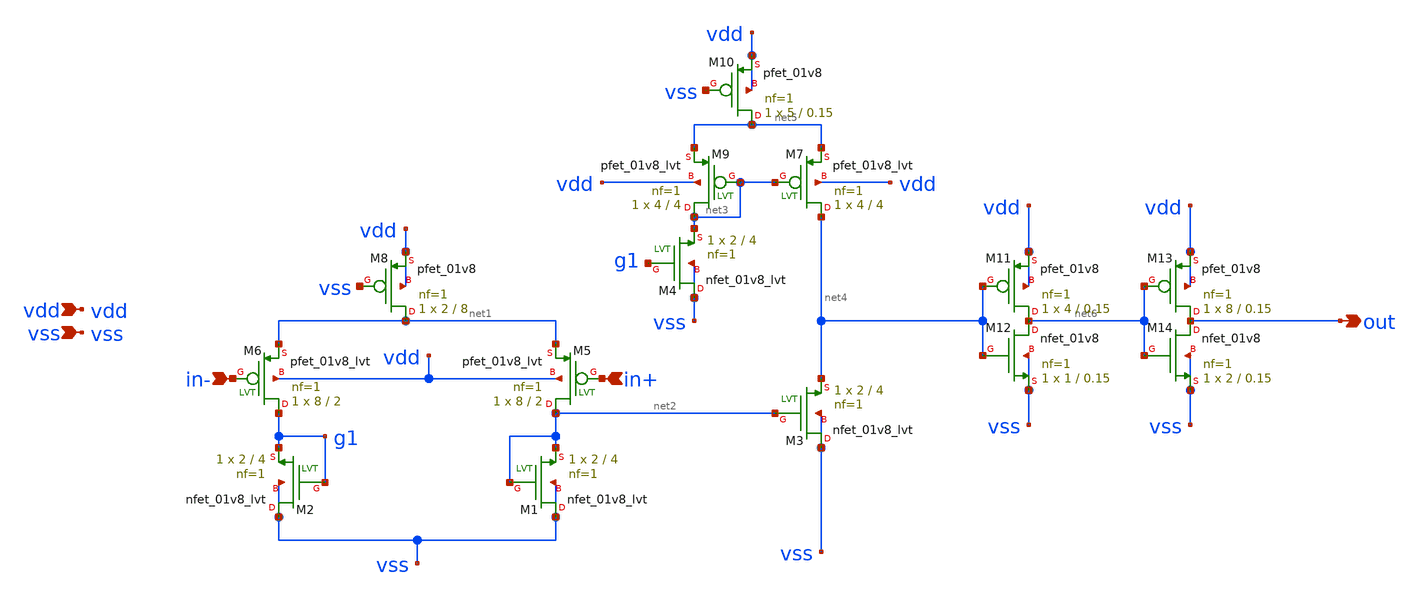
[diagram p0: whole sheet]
** sch_path: custom_gds/tt_um_tim2305_adc_dac/xschem/compr2.sch
**.subckt compr2 in- out in+ vdd vss
*.ipin in-
*.opin out
*.ipin in+
*.ipin vdd
*.ipin vss
XM1 vss net2 net2 vss sky130_fd_pr__nfet_01v8_lvt L=4 W=2 nf=1 ad='int((nf+1)/2) * W/nf * 0.29' as='int((nf+2)/2) * W/nf * 0.29'
+ pd='2*int((nf+1)/2) * (W/nf + 0.29)' ps='2*int((nf+2)/2) * (W/nf + 0.29)' nrd='0.29 / W' nrs='0.29 / W'
+ sa=0 sb=0 sd=0 mult=1 m=1
XM2 vss g1 g1 vss sky130_fd_pr__nfet_01v8_lvt L=4 W=2 nf=1 ad='int((nf+1)/2) * W/nf * 0.29' as='int((nf+2)/2) * W/nf * 0.29'
+ pd='2*int((nf+1)/2) * (W/nf + 0.29)' ps='2*int((nf+2)/2) * (W/nf + 0.29)' nrd='0.29 / W' nrs='0.29 / W'
+ sa=0 sb=0 sd=0 mult=1 m=1
XM3 vss net2 net4 vss sky130_fd_pr__nfet_01v8_lvt L=4 W=2 nf=1 ad='int((nf+1)/2) * W/nf * 0.29' as='int((nf+2)/2) * W/nf * 0.29'
+ pd='2*int((nf+1)/2) * (W/nf + 0.29)' ps='2*int((nf+2)/2) * (W/nf + 0.29)' nrd='0.29 / W' nrs='0.29 / W'
+ sa=0 sb=0 sd=0 mult=1 m=1
XM4 vss g1 net3 vss sky130_fd_pr__nfet_01v8_lvt L=4 W=2 nf=1 ad='int((nf+1)/2) * W/nf * 0.29' as='int((nf+2)/2) * W/nf * 0.29'
+ pd='2*int((nf+1)/2) * (W/nf + 0.29)' ps='2*int((nf+2)/2) * (W/nf + 0.29)' nrd='0.29 / W' nrs='0.29 / W'
+ sa=0 sb=0 sd=0 mult=1 m=1
XM5 net2 in+ net1 vdd sky130_fd_pr__pfet_01v8_lvt L=2 W=8 nf=1 ad='int((nf+1)/2) * W/nf * 0.29' as='int((nf+2)/2) * W/nf * 0.29'
+ pd='2*int((nf+1)/2) * (W/nf + 0.29)' ps='2*int((nf+2)/2) * (W/nf + 0.29)' nrd='0.29 / W' nrs='0.29 / W'
+ sa=0 sb=0 sd=0 mult=1 m=1
XM6 g1 in- net1 vdd sky130_fd_pr__pfet_01v8_lvt L=2 W=8 nf=1 ad='int((nf+1)/2) * W/nf * 0.29' as='int((nf+2)/2) * W/nf * 0.29'
+ pd='2*int((nf+1)/2) * (W/nf + 0.29)' ps='2*int((nf+2)/2) * (W/nf + 0.29)' nrd='0.29 / W' nrs='0.29 / W'
+ sa=0 sb=0 sd=0 mult=1 m=1
XM7 net4 net3 net5 vdd sky130_fd_pr__pfet_01v8_lvt L=4 W=4 nf=1 ad='int((nf+1)/2) * W/nf * 0.29' as='int((nf+2)/2) * W/nf * 0.29'
+ pd='2*int((nf+1)/2) * (W/nf + 0.29)' ps='2*int((nf+2)/2) * (W/nf + 0.29)' nrd='0.29 / W' nrs='0.29 / W'
+ sa=0 sb=0 sd=0 mult=1 m=1
XM9 net3 net3 net5 vdd sky130_fd_pr__pfet_01v8_lvt L=4 W=4 nf=1 ad='int((nf+1)/2) * W/nf * 0.29' as='int((nf+2)/2) * W/nf * 0.29'
+ pd='2*int((nf+1)/2) * (W/nf + 0.29)' ps='2*int((nf+2)/2) * (W/nf + 0.29)' nrd='0.29 / W' nrs='0.29 / W'
+ sa=0 sb=0 sd=0 mult=1 m=1
XM8 net1 vss vdd vdd sky130_fd_pr__pfet_01v8 L=8 W=2 nf=1 ad='int((nf+1)/2) * W/nf * 0.29' as='int((nf+2)/2) * W/nf * 0.29'
+ pd='2*int((nf+1)/2) * (W/nf + 0.29)' ps='2*int((nf+2)/2) * (W/nf + 0.29)' nrd='0.29 / W' nrs='0.29 / W'
+ sa=0 sb=0 sd=0 mult=1 m=1
XM10 net5 vss vdd vdd sky130_fd_pr__pfet_01v8 L=0.15 W=5 nf=1 ad='int((nf+1)/2) * W/nf * 0.29' as='int((nf+2)/2) * W/nf * 0.29'
+ pd='2*int((nf+1)/2) * (W/nf + 0.29)' ps='2*int((nf+2)/2) * (W/nf + 0.29)' nrd='0.29 / W' nrs='0.29 / W'
+ sa=0 sb=0 sd=0 mult=1 m=1
XM11 net6 net4 vdd vdd sky130_fd_pr__pfet_01v8 L=0.15 W=4 nf=1 ad='int((nf+1)/2) * W/nf * 0.29' as='int((nf+2)/2) * W/nf * 0.29'
+ pd='2*int((nf+1)/2) * (W/nf + 0.29)' ps='2*int((nf+2)/2) * (W/nf + 0.29)' nrd='0.29 / W' nrs='0.29 / W'
+ sa=0 sb=0 sd=0 mult=1 m=1
XM12 net6 net4 vss vss sky130_fd_pr__nfet_01v8 L=0.15 W=1 nf=1 ad='int((nf+1)/2) * W/nf * 0.29' as='int((nf+2)/2) * W/nf * 0.29'
+ pd='2*int((nf+1)/2) * (W/nf + 0.29)' ps='2*int((nf+2)/2) * (W/nf + 0.29)' nrd='0.29 / W' nrs='0.29 / W'
+ sa=0 sb=0 sd=0 mult=1 m=1
XM13 out net6 vdd vdd sky130_fd_pr__pfet_01v8 L=0.15 W=8 nf=1 ad='int((nf+1)/2) * W/nf * 0.29' as='int((nf+2)/2) * W/nf * 0.29'
+ pd='2*int((nf+1)/2) * (W/nf + 0.29)' ps='2*int((nf+2)/2) * (W/nf + 0.29)' nrd='0.29 / W' nrs='0.29 / W'
+ sa=0 sb=0 sd=0 mult=1 m=1
XM14 out net6 vss vss sky130_fd_pr__nfet_01v8 L=0.15 W=2 nf=1 ad='int((nf+1)/2) * W/nf * 0.29' as='int((nf+2)/2) * W/nf * 0.29'
+ pd='2*int((nf+1)/2) * (W/nf + 0.29)' ps='2*int((nf+2)/2) * (W/nf + 0.29)' nrd='0.29 / W' nrs='0.29 / W'
+ sa=0 sb=0 sd=0 mult=1 m=1
**.ends
.end
